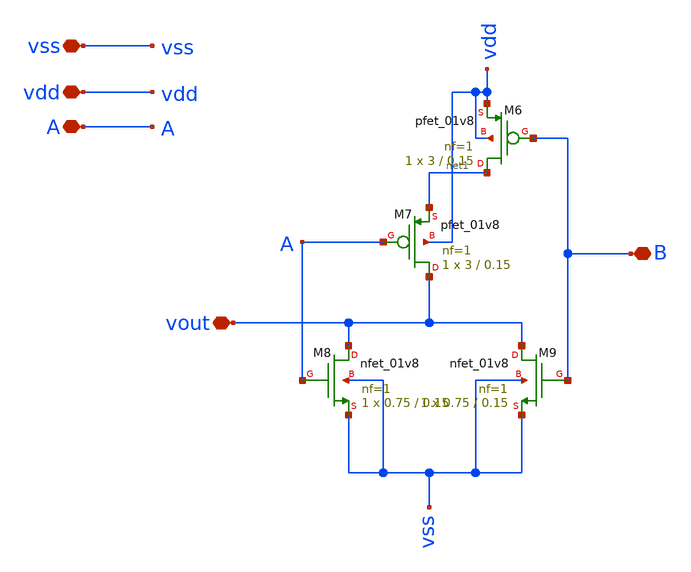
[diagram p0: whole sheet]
** sch_path: sch/NOR.sch
**.subckt NOR A vdd vss vout B
*.iopin A
*.iopin vdd
*.iopin vss
*.iopin vout
*.iopin B
XM8 vout A vss vss sky130_fd_pr__nfet_01v8 L=0.15 W=0.75 nf=1 ad='int((1 + 1)/2) * 0.75 / 1 * 0.29' as='int((1 + 2)/2) * 0.75 / 1 * 0.29'
+ pd='2*int((1 + 1)/2) * (0.75 / 1 + 0.29)' ps='2*int((1 + 2)/2) * (0.75 / 1 + 0.29)' nrd='0.29 / 0.75 '
+ nrs='0.29 / 0.75 ' sa=0 sb=0 sd=0 mult=1 m=1
XM9 vout B vss vss sky130_fd_pr__nfet_01v8 L=0.15 W=0.75 nf=1 ad='int((1 + 1)/2) * 0.75 / 1 * 0.29' as='int((1 + 2)/2) * 0.75 / 1 * 0.29'
+ pd='2*int((1 + 1)/2) * (0.75 / 1 + 0.29)' ps='2*int((1 + 2)/2) * (0.75 / 1 + 0.29)' nrd='0.29 / 0.75 '
+ nrs='0.29 / 0.75 ' sa=0 sb=0 sd=0 mult=1 m=1
XM7 vout A net1 vdd sky130_fd_pr__pfet_01v8 L=0.15 W=3 nf=1 ad='int((nf+1)/2) * W/nf * 0.29' as='int((nf+2)/2) * W/nf * 0.29'
+ pd='2*int((nf+1)/2) * (W/nf + 0.29)' ps='2*int((nf+2)/2) * (W/nf + 0.29)' nrd='0.29 / W' nrs='0.29 / W'
+ sa=0 sb=0 sd=0 mult=1 m=1
XM6 net1 B vdd vdd sky130_fd_pr__pfet_01v8 L=0.15 W=3 nf=1 ad='int((nf+1)/2) * W/nf * 0.29' as='int((nf+2)/2) * W/nf * 0.29'
+ pd='2*int((nf+1)/2) * (W/nf + 0.29)' ps='2*int((nf+2)/2) * (W/nf + 0.29)' nrd='0.29 / W' nrs='0.29 / W'
+ sa=0 sb=0 sd=0 mult=1 m=1
**.ends
.end
